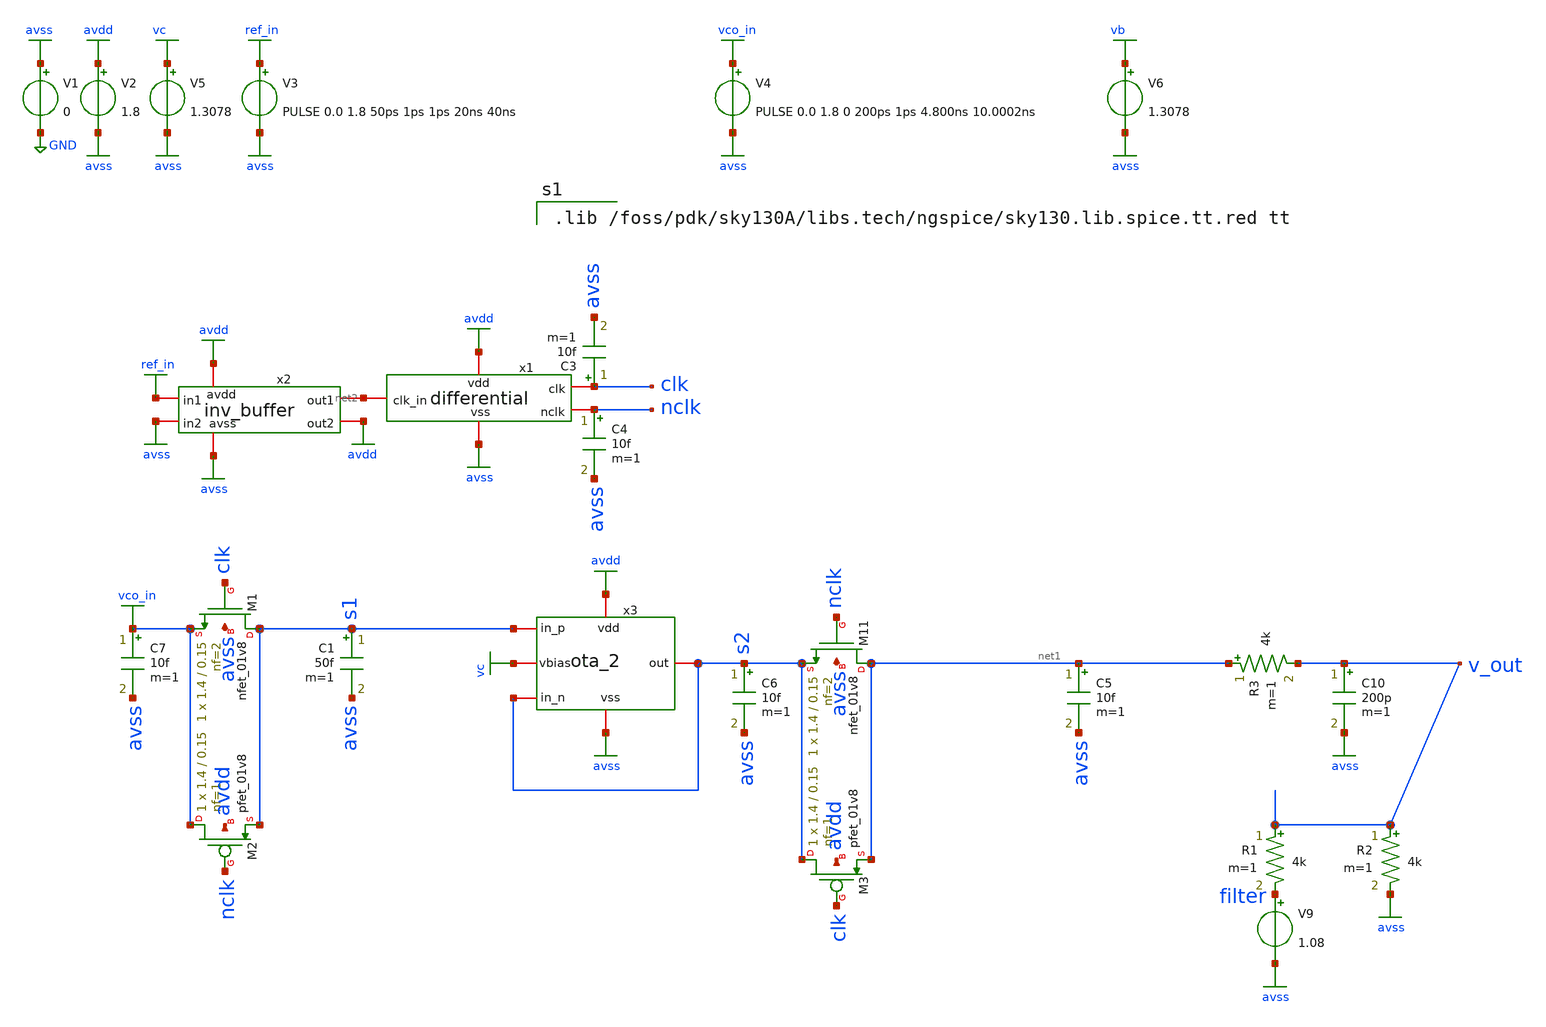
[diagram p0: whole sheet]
** sch_path: xschem/sspd_sim1.sch
**.subckt sspd_sim1
V1 avss GND 0
V2 avdd avss 1.8
V3 ref_in avss PULSE 0.0 1.8 50ps 1ps 1ps 20ns 40ns
V5 vc avss 1.3078
x1 avdd avss net2 clk nclk differential
x2 avdd avss net2 avdd avss ref_in inv_buffer
x3 avdd avss s1 s2 s2 vc ota_2
C1 s1 avss 50f m=1
XM11 net1 nclk s2 avss sky130_fd_pr__nfet_01v8 L=0.15 W=1.4 nf=2 ad='int((nf+1)/2) * W/nf * 0.29' as='int((nf+2)/2) * W/nf * 0.29'
+ pd='2*int((nf+1)/2) * (W/nf + 0.29)' ps='2*int((nf+2)/2) * (W/nf + 0.29)' nrd='0.29 / W' nrs='0.29 / W'
+ sa=0 sb=0 sd=0 mult=1 m=1
XM1 s1 clk vco_in avss sky130_fd_pr__nfet_01v8 L=0.15 W=1.4 nf=2 ad='int((nf+1)/2) * W/nf * 0.29' as='int((nf+2)/2) * W/nf * 0.29'
+ pd='2*int((nf+1)/2) * (W/nf + 0.29)' ps='2*int((nf+2)/2) * (W/nf + 0.29)' nrd='0.29 / W' nrs='0.29 / W'
+ sa=0 sb=0 sd=0 mult=1 m=1
V4 vco_in avss PULSE 0.0 1.8 0 200ps 1ps 4.800ns 10.0002ns
C3 clk avss 10f m=1
C4 nclk avss 10f m=1
C6 s2 avss 10f m=1
C7 vco_in avss 10f m=1
XM2 vco_in nclk s1 avdd sky130_fd_pr__pfet_01v8 L=0.15 W=1.4 nf=1 ad='int((nf+1)/2) * W/nf * 0.29' as='int((nf+2)/2) * W/nf * 0.29'
+ pd='2*int((nf+1)/2) * (W/nf + 0.29)' ps='2*int((nf+2)/2) * (W/nf + 0.29)' nrd='0.29 / W' nrs='0.29 / W'
+ sa=0 sb=0 sd=0 mult=1 m=1
XM3 s2 clk net1 avdd sky130_fd_pr__pfet_01v8 L=0.15 W=1.4 nf=1 ad='int((nf+1)/2) * W/nf * 0.29' as='int((nf+2)/2) * W/nf * 0.29'
+ pd='2*int((nf+1)/2) * (W/nf + 0.29)' ps='2*int((nf+2)/2) * (W/nf + 0.29)' nrd='0.29 / W' nrs='0.29 / W'
+ sa=0 sb=0 sd=0 mult=1 m=1
V6 vb avss 1.3078
C5 net1 avss 10f m=1
R1 v_out filter 4k m=1
V9 filter avss 1.08
R2 v_out avss 4k m=1
C10 v_out avss 200p m=1
R3 net1 v_out 4k m=1
**** begin user architecture code

.lib /foss/pdk/sky130A/libs.tech/ngspice/sky130.lib.spice.tt.red tt



.control
save ref_in vco_in clk nclk v_out @V1[i] @V3[i] s1 s2
tran 0.005n 30000n 0n
run
*plot clk nclk xlimit 40n 160n
*plot ref_in vco_in xlimit 0n 160n
*plot s1 v_out
*plot s1
plot ref_in vco_in
plot v_out
*fft vco_in
*plot db(mag(vco_in)) xlimit 0.1meg 200meg ylimit 0.0 -60
*plot v_out
*plot clk nclk s1 s2 v_out
*plot s2
*plot s1 s2
*plot @V1[i] @V3[i]
*compose values values 10.738n 10.666n 10.596n
*foreach val $&values
*	echo run = $val
*	alter @v4[pulse] = [ 1.8 0.0 0 5ps 5ps 5.323ns $val ] $ vector
*	save ref_in vco_in clk nclk v_out @V1[i] @V3[i] s1 s2
*	tran 0.001n 280n 40n
*	run
*end
*plot tran1.vco_in tran2.vco_in tran3.vco_in
*plot tran1.s2 tran2.s2 tran3.s2
*plot tran1.v_out tran2.v_out tran3.v_out
*plot tran1.v_out
*plot tran2.v_out
*plot tran3.v_out
*plot tran1.s2
*plot tran2.s2
*plot tran3.s2
*compose values start=0.0 stop=1.8 step=0.1
*foreach val $&values
*	echo run = $val
*	alter v5 $val
*	save ref_in vco_in clk nclk v_out @V1[i] @V3[i] s1 s2
*	tran 0.05n 280n 40n
*	run
*end
.endc
.end


**** end user architecture code
**.ends
.GLOBAL avdd
.GLOBAL avss
.GLOBAL GND
.GLOBAL ref_in
.GLOBAL vc
.GLOBAL vco_in
.GLOBAL vb
.end
